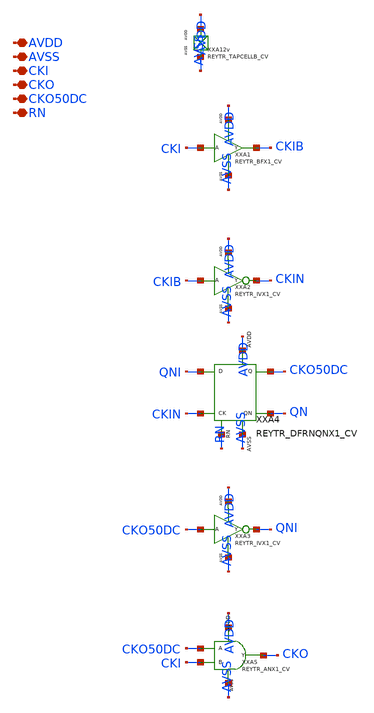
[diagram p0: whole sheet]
** sch_path: design/REY_TR_SKY130A/REYTR_CKDIV2_CV.sch
**.subckt REYTR_CKDIV2_CV AVDD AVSS CKI CKO CKO50DC RN
*.iopin AVDD
*.iopin AVSS
*.iopin CKI
*.iopin CKO
*.iopin CKO50DC
*.iopin RN
XXA12v AVDD AVSS REYTR_TAPCELLB_CV xoffset=0 yoffset=0 angle=0
XXA2 CKIB CKIN AVDD AVSS REYTR_IVX1_CV
XXA4 QNI CKIN RN CKO50DC QN AVDD AVSS REYTR_DFRNQNX1_CV xoffset=0 yoffset=0 angle=0
XXA3 CKO50DC QNI AVDD AVSS REYTR_IVX1_CV
XXA5 CKO50DC CKI CKO AVDD AVSS REYTR_ANX1_CV xoffset=0 yoffset=0 angle=0 M=1
**.ends
.end
